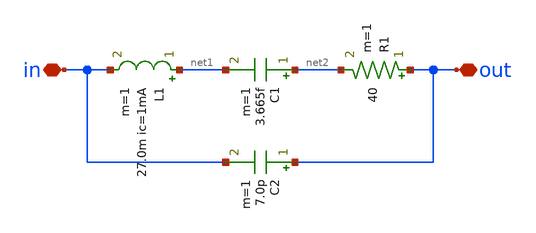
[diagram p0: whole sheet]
** sch_path: archive/resonator_32k.sch
**.subckt resonator_32k out in
*.iopin out
*.iopin in
L1 net1 in 27.0m ic=1mA m=1
C1 net2 net1 3.665f m=1
C2 out in 7.0p m=1
R1 out net2 40 m=1
**.ends
.end
